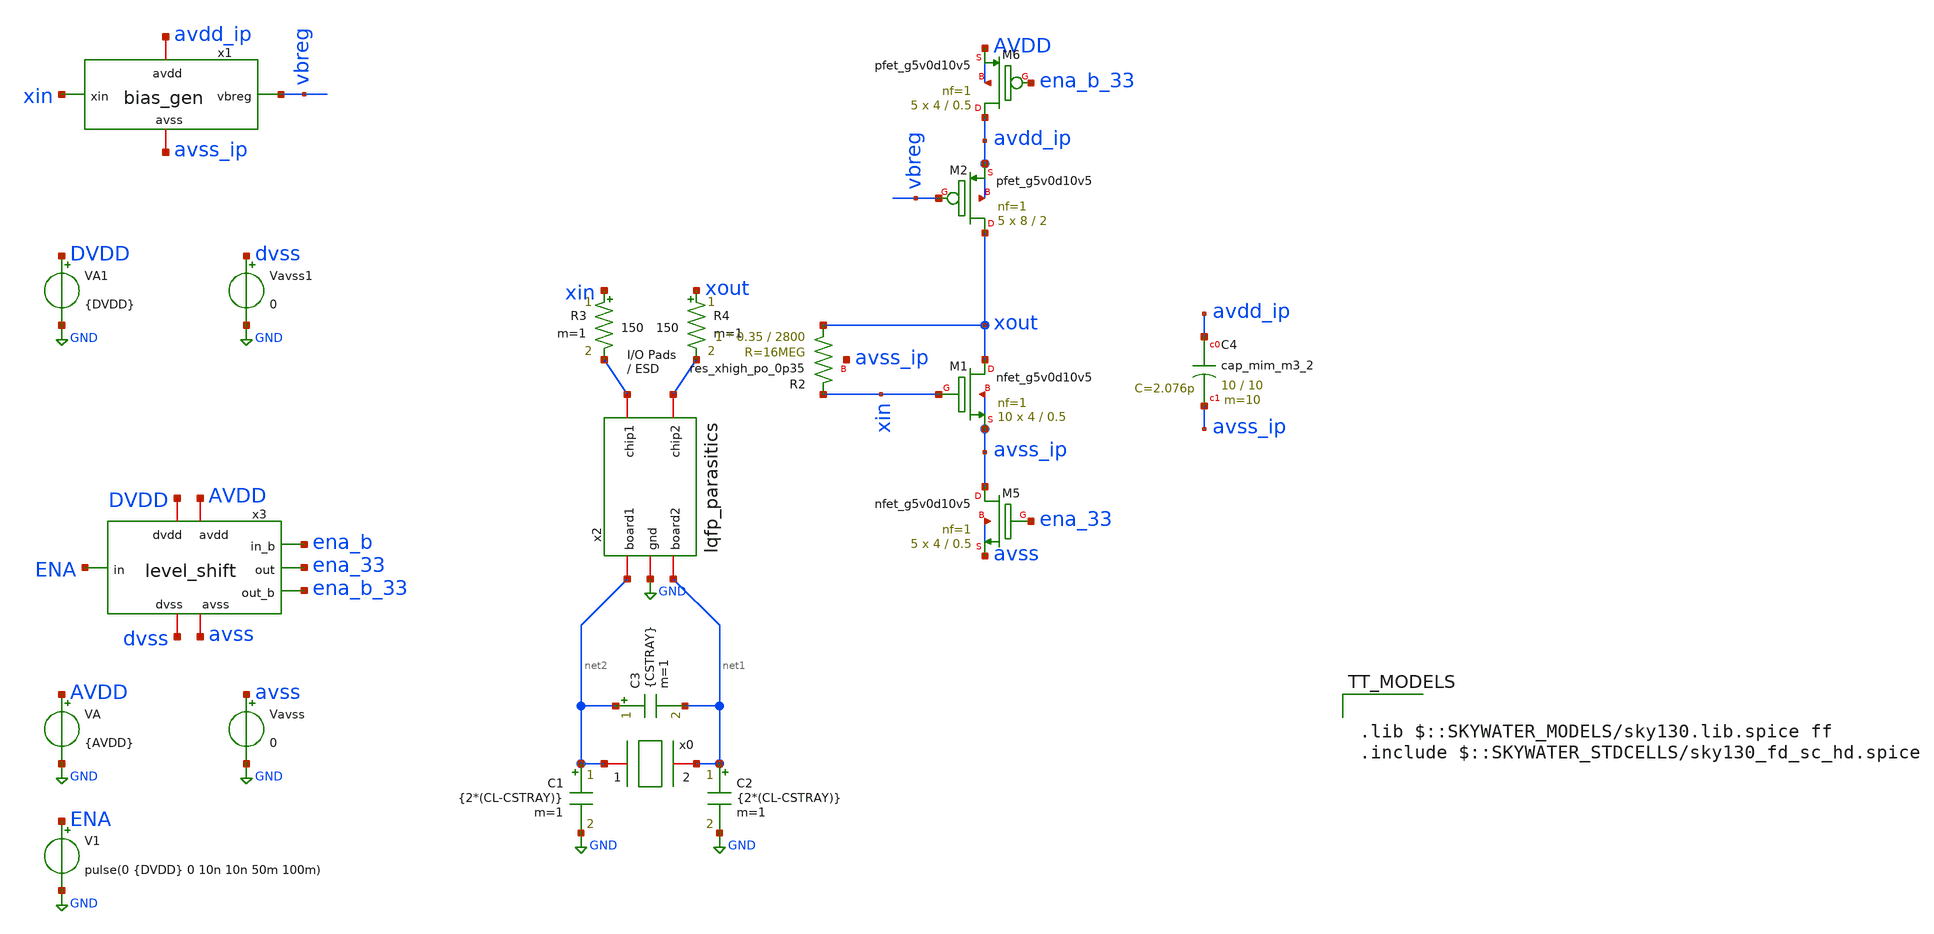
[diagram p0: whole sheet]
** sch_path: xschem/tb_man__bias.sch

.lib $::SKYWATER_MODELS/sky130.lib.spice ff
.include $::SKYWATER_STDCELLS/sky130_fd_sc_hd.spice

**.subckt tb_man__bias
VA AVDD GND {AVDD}
C1 net2 GND {2*(CL-CSTRAY)} m=1
C2 net1 GND {2*(CL-CSTRAY)} m=1
C3 net2 net1 {CSTRAY} m=1
R3 xin net3 150 m=1
R4 xout net4 150 m=1
x2 net4 net3 GND net2 net1 lqfp_parasitics
V1 ENA GND pulse(0 {DVDD} 0 10n 10n 50m 100m)
x0 net2 net1 xtal_iqd_125_1
Vavss avss GND 0
x3 AVDD DVDD ena_33 ena_b_33 ENA dvss avss ena_b level_shift
XM1 xout xin avss_ip avss_ip sky130_fd_pr__nfet_g5v0d10v5 L=0.5 W=4 nf=1 ad='int((nf+1)/2) * W/nf * 0.29'
+ as='int((nf+2)/2) * W/nf * 0.29' pd='2*int((nf+1)/2) * (W/nf + 0.29)' ps='2*int((nf+2)/2) * (W/nf + 0.29)'
+ nrd='0.29 / W' nrs='0.29 / W' sa=0 sb=0 sd=0 mult=10 m=10
XM2 xout vbreg avdd_ip avdd_ip sky130_fd_pr__pfet_g5v0d10v5 L=2 W=8 nf=1 ad='int((nf+1)/2) * W/nf * 0.29'
+ as='int((nf+2)/2) * W/nf * 0.29' pd='2*int((nf+1)/2) * (W/nf + 0.29)' ps='2*int((nf+2)/2) * (W/nf + 0.29)'
+ nrd='0.29 / W' nrs='0.29 / W' sa=0 sb=0 sd=0 mult=5 m=5
XM5 avss_ip ena_33 avss avss sky130_fd_pr__nfet_g5v0d10v5 L=0.5 W=4 nf=1 ad='int((nf+1)/2) * W/nf * 0.29'
+ as='int((nf+2)/2) * W/nf * 0.29' pd='2*int((nf+1)/2) * (W/nf + 0.29)' ps='2*int((nf+2)/2) * (W/nf + 0.29)'
+ nrd='0.29 / W' nrs='0.29 / W' sa=0 sb=0 sd=0 mult=5 m=5
XM6 avdd_ip ena_b_33 AVDD AVDD sky130_fd_pr__pfet_g5v0d10v5 L=0.5 W=4 nf=1 ad='int((nf+1)/2) * W/nf * 0.29'
+ as='int((nf+2)/2) * W/nf * 0.29' pd='2*int((nf+1)/2) * (W/nf + 0.29)' ps='2*int((nf+2)/2) * (W/nf + 0.29)'
+ nrd='0.29 / W' nrs='0.29 / W' sa=0 sb=0 sd=0 mult=5 m=5
XR2 xout xin avss_ip sky130_fd_pr__res_xhigh_po_0p35 L=2800 mult=1 m=1
x1 avdd_ip vbreg xin avss_ip bias_gen
XC4 avdd_ip avss_ip sky130_fd_pr__cap_mim_m3_2 W=10 L=10 MF=10 m=10
VA1 DVDD GND {DVDD}
Vavss1 dvss GND 0
**** begin user architecture code

.param DVDD=1.8
.param AVDD=5.5
.param ENA=1
.param STANDBY=0
.param CL=12.5p
.param CSTRAY=2p
.model DUMMY D()
.option TEMP=-40
.control
  *save V(XIN) V(XOUT)
  *save V(vbreg) V(x1.vg1) V(x1.vg2) V(x1.icnode)
  *save I(VA)
  save all
  tran 25n 5m
  *tran 1n 0.2m
  remzerovec
  write tb_lsxo_general_short.raw
  plot V(vbreg) V(x1.vg1) V(x1.vg2) V(x1.icnode)
  plot V(XIN) V(XOUT)
  *plot I(VA)
  plot @m.xm1.msky130_fd_pr__nfet_g5v0d10v5[id] @m.x1.xm2.msky130_fd_pr__nfet_g5v0d10v5[id]
  plot @m.xm1.msky130_fd_pr__nfet_g5v0d10v5[gm]
  * quit 0
.endc

**** end user architecture code
**.ends
.GLOBAL GND
.end
